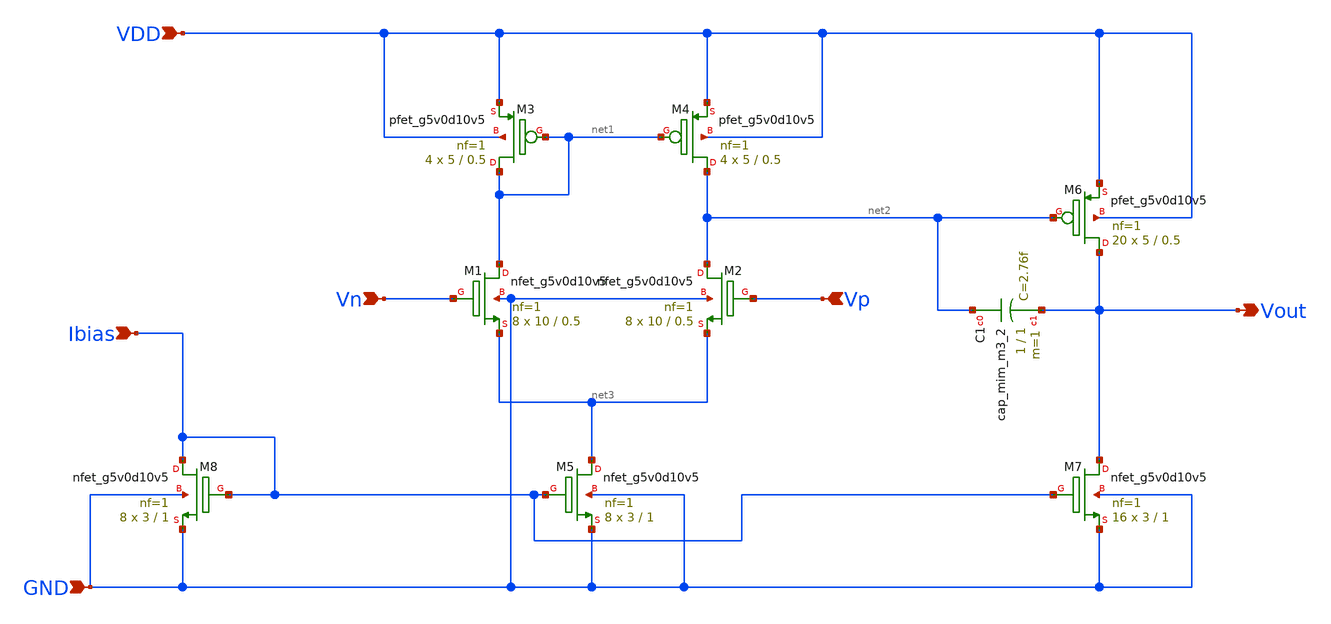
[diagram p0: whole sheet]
** sch_path: Analog_blocks/Analog_Blocks/OTA/Schematic/Miller_OTA/Transistor5v/Miller_OTA_NMOS.sch
**.subckt Miller_OTA_NMOS VDD Ibias Vn Vp Vout GND
*.ipin VDD
*.ipin Ibias
*.ipin Vn
*.ipin Vp
*.opin Vout
*.ipin GND
XM1 net1 Vn net3 GND sky130_fd_pr__nfet_g5v0d10v5 L=0.5 W=10 nf=1 ad='int((nf+1)/2) * W/nf * 0.29' as='int((nf+2)/2) * W/nf * 0.29'
+ pd='2*int((nf+1)/2) * (W/nf + 0.29)' ps='2*int((nf+2)/2) * (W/nf + 0.29)' nrd='0.29 / W' nrs='0.29 / W'
+ sa=0 sb=0 sd=0 mult=8 m=8
XM2 net2 Vp net3 GND sky130_fd_pr__nfet_g5v0d10v5 L=0.5 W=10 nf=1 ad='int((nf+1)/2) * W/nf * 0.29' as='int((nf+2)/2) * W/nf * 0.29'
+ pd='2*int((nf+1)/2) * (W/nf + 0.29)' ps='2*int((nf+2)/2) * (W/nf + 0.29)' nrd='0.29 / W' nrs='0.29 / W'
+ sa=0 sb=0 sd=0 mult=8 m=8
XM3 net1 net1 VDD VDD sky130_fd_pr__pfet_g5v0d10v5 L=0.5 W=5 nf=1 ad='int((nf+1)/2) * W/nf * 0.29' as='int((nf+2)/2) * W/nf * 0.29'
+ pd='2*int((nf+1)/2) * (W/nf + 0.29)' ps='2*int((nf+2)/2) * (W/nf + 0.29)' nrd='0.29 / W' nrs='0.29 / W'
+ sa=0 sb=0 sd=0 mult=4 m=4
XM4 net2 net1 VDD VDD sky130_fd_pr__pfet_g5v0d10v5 L=0.5 W=5 nf=1 ad='int((nf+1)/2) * W/nf * 0.29' as='int((nf+2)/2) * W/nf * 0.29'
+ pd='2*int((nf+1)/2) * (W/nf + 0.29)' ps='2*int((nf+2)/2) * (W/nf + 0.29)' nrd='0.29 / W' nrs='0.29 / W'
+ sa=0 sb=0 sd=0 mult=4 m=4
XM6 Vout net2 VDD VDD sky130_fd_pr__pfet_g5v0d10v5 L=0.5 W=5 nf=1 ad='int((nf+1)/2) * W/nf * 0.29' as='int((nf+2)/2) * W/nf * 0.29'
+ pd='2*int((nf+1)/2) * (W/nf + 0.29)' ps='2*int((nf+2)/2) * (W/nf + 0.29)' nrd='0.29 / W' nrs='0.29 / W'
+ sa=0 sb=0 sd=0 mult=20 m=20
XM5 net3 Ibias GND GND sky130_fd_pr__nfet_g5v0d10v5 L=1 W=3 nf=1 ad='int((nf+1)/2) * W/nf * 0.29' as='int((nf+2)/2) * W/nf * 0.29'
+ pd='2*int((nf+1)/2) * (W/nf + 0.29)' ps='2*int((nf+2)/2) * (W/nf + 0.29)' nrd='0.29 / W' nrs='0.29 / W'
+ sa=0 sb=0 sd=0 mult=8 m=8
XM8 Ibias Ibias GND GND sky130_fd_pr__nfet_g5v0d10v5 L=1 W=3 nf=1 ad='int((nf+1)/2) * W/nf * 0.29' as='int((nf+2)/2) * W/nf * 0.29'
+ pd='2*int((nf+1)/2) * (W/nf + 0.29)' ps='2*int((nf+2)/2) * (W/nf + 0.29)' nrd='0.29 / W' nrs='0.29 / W'
+ sa=0 sb=0 sd=0 mult=8 m=8
XM7 Vout Ibias GND GND sky130_fd_pr__nfet_g5v0d10v5 L=1 W=3 nf=1 ad='int((nf+1)/2) * W/nf * 0.29' as='int((nf+2)/2) * W/nf * 0.29'
+ pd='2*int((nf+1)/2) * (W/nf + 0.29)' ps='2*int((nf+2)/2) * (W/nf + 0.29)' nrd='0.29 / W' nrs='0.29 / W'
+ sa=0 sb=0 sd=0 mult=16 m=16
XC1 net2 Vout sky130_fd_pr__cap_mim_m3_2 W=1 L=1 MF=1 m=1
**.ends
.end
